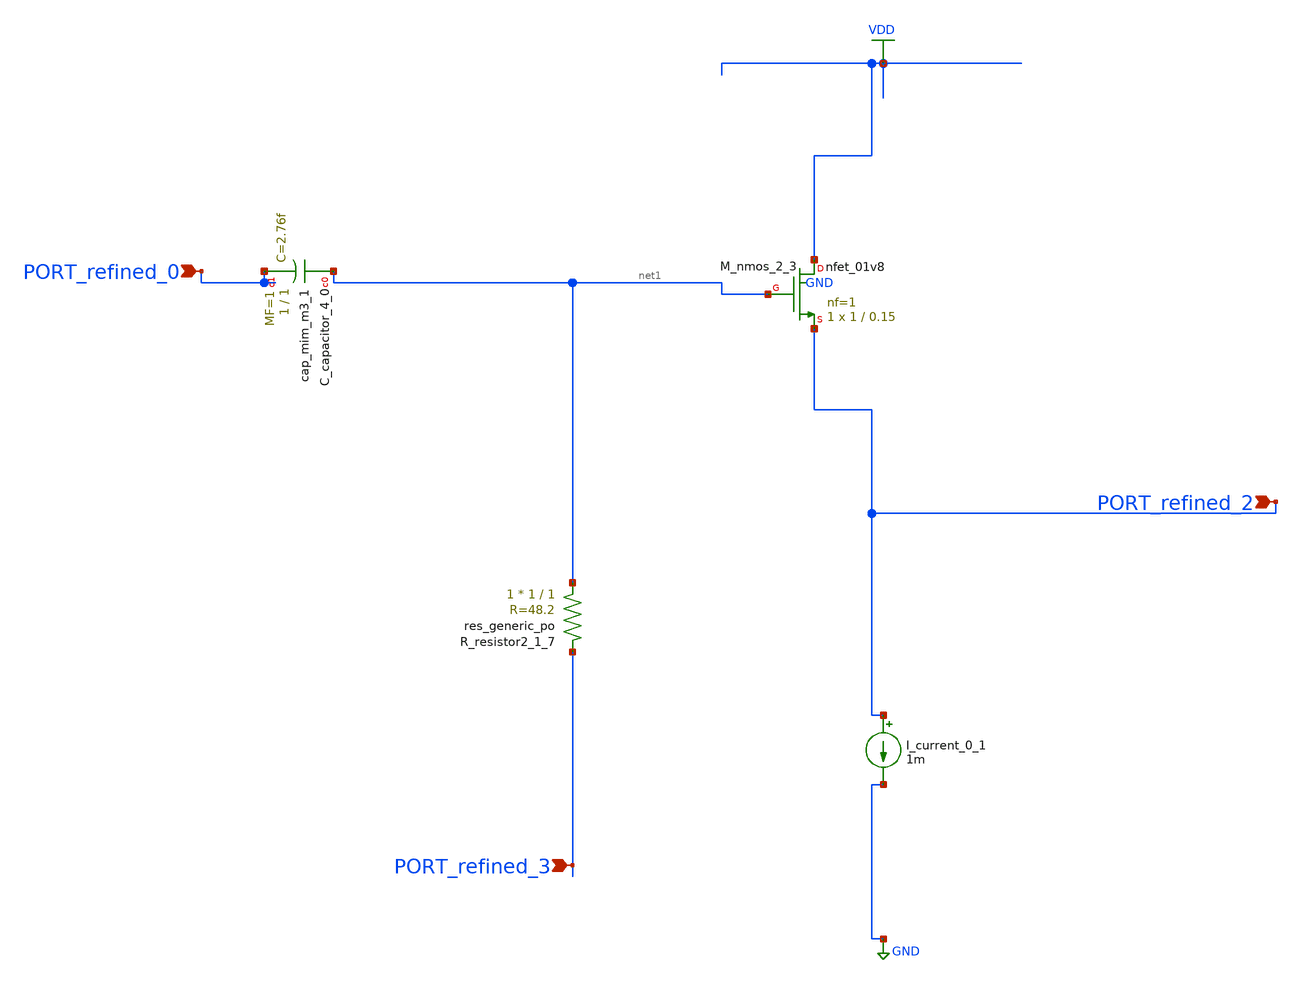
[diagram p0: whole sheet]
** sch_path: schematics/SchemGen/10_1016_j_aeue_2023_154777_03_001.sch
**.subckt 10_1016_j_aeue_2023_154777_03_001 PORT_refined_3 PORT_refined_0 PORT_refined_2
*.ipin PORT_refined_3
*.ipin PORT_refined_0
*.ipin PORT_refined_2
XC_capacitor_4_0 net1 PORT_refined_0 sky130_fd_pr__cap_mim_m3_1 W=1 L=1 MF=1 m=1
I_current_0_1 PORT_refined_2 GND 1m
XM_nmos_2_3 VDD net1 PORT_refined_2 GND sky130_fd_pr__nfet_01v8 L=0.15 W=1 nf=1 ad='int((1 + 1)/2) * 1 / 1 * 0.29'
+ as='int((1 + 2)/2) * 1 / 1 * 0.29' pd='2*int((1 + 1)/2) * (1 / 1 + 0.29)' ps='2*int((1 + 2)/2) * (1 / 1 + 0.29)'
+ nrd='0.29 / 1 ' nrs='0.29 / 1 ' sa=0 sb=0 sd=0 mult=1 m=1
XR_resistor2_1_7 net1 PORT_refined_3 sky130_fd_pr__res_generic_po W=1 L=1 m=1
**.ends
.GLOBAL GND
.GLOBAL VDD
.end
